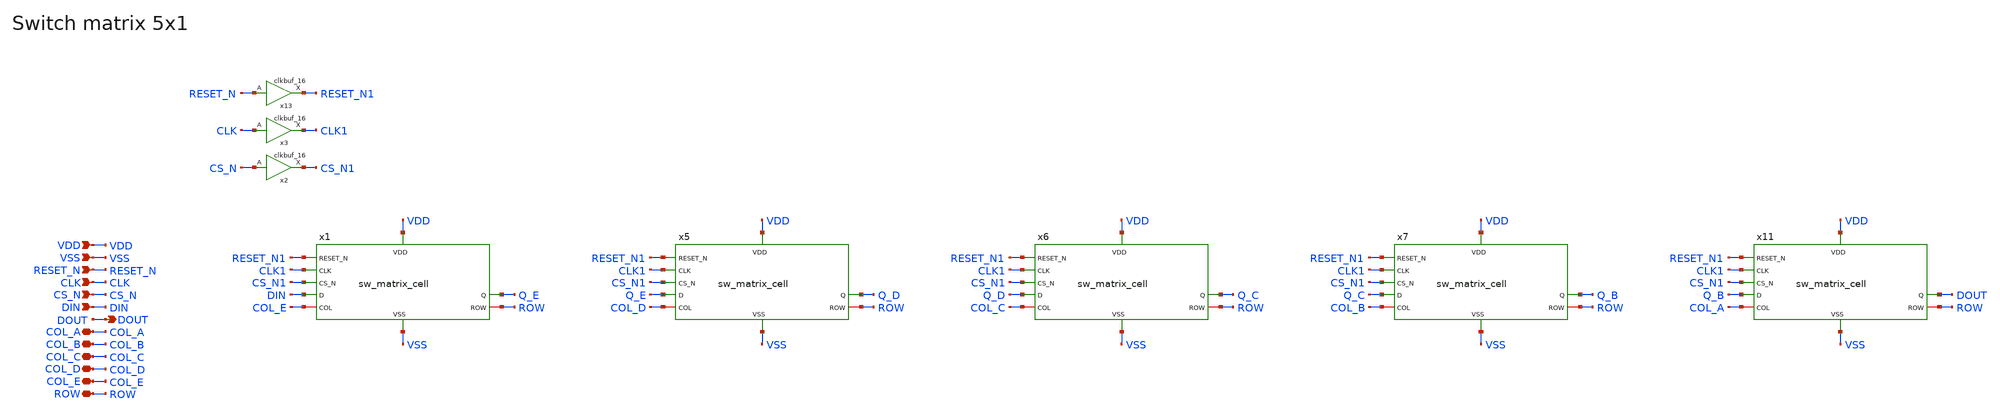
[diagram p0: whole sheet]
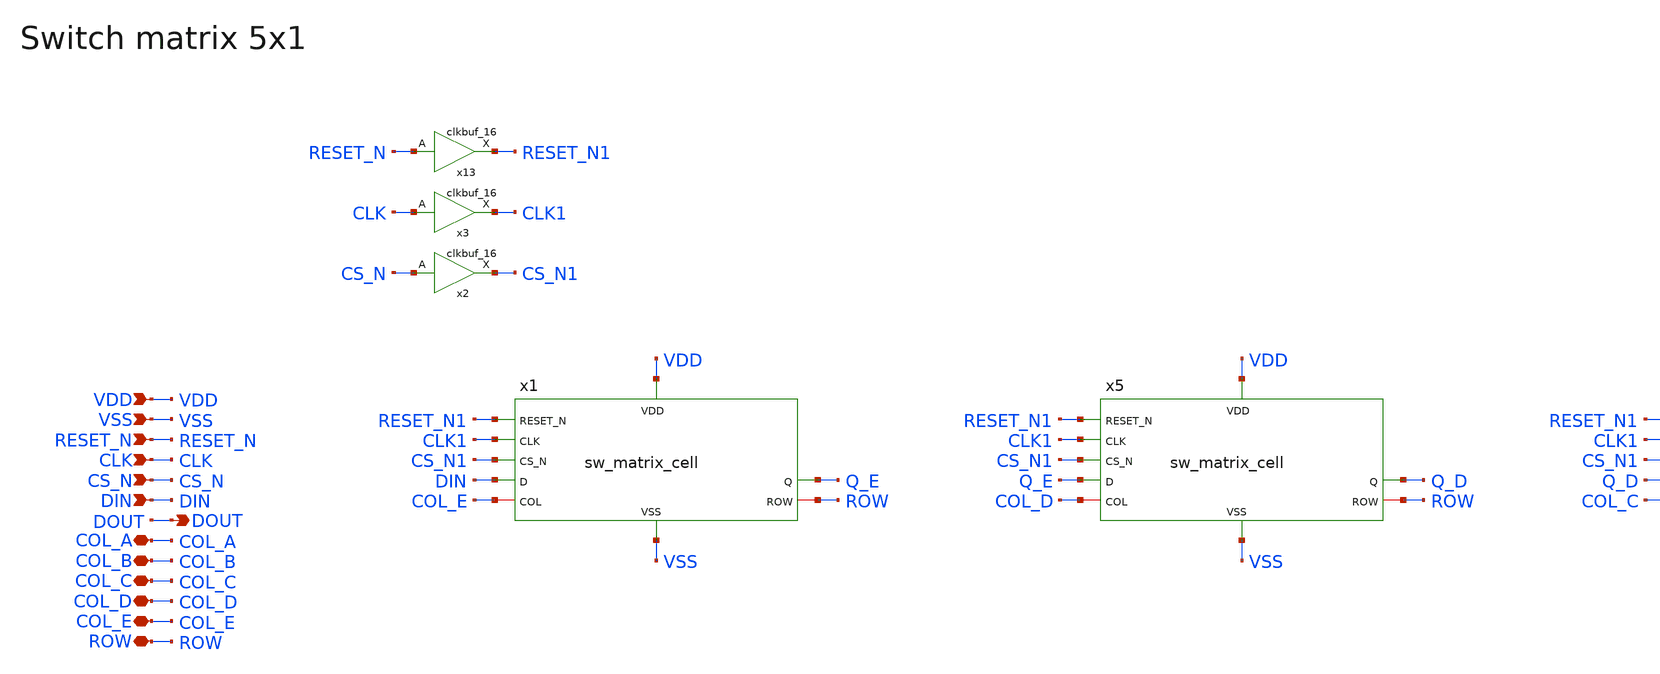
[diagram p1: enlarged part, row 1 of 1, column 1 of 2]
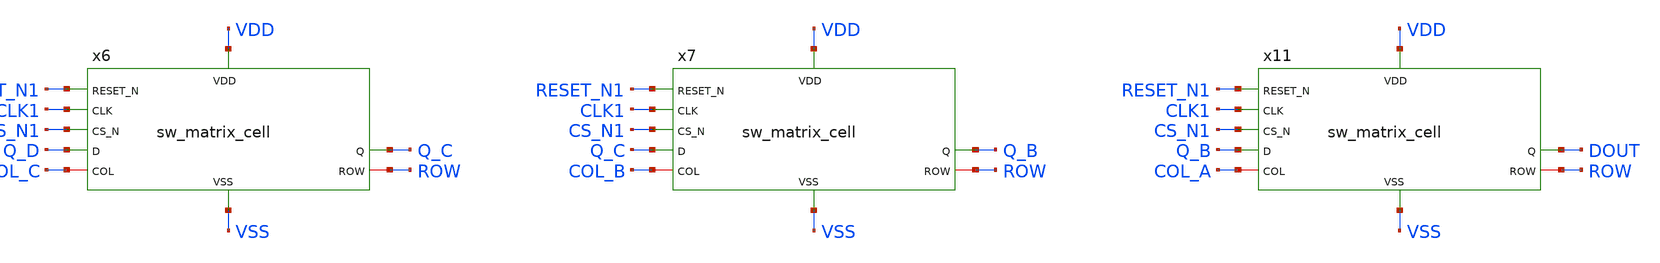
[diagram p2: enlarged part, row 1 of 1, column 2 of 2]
** sch_path: designs/libs/core_analog/sw_matrix/sw_matrix_5x1.sch
* Copyright 2022 GlobalFoundries PDK Authors
* Licensed under the Apache License, Version 2.0 (the "License");
* you may not use this file except in compliance with the License.
* You may obtain a copy of the License at
* https://www.apache.org/licenses/LICENSE-2.0
* Unless required by applicable law or agreed to in writing, software
* distributed under the License is distributed on an "AS IS" BASIS,
* WITHOUT WARRANTIES OR CONDITIONS OF ANY KIND, either express or implied.
* See the License for the specific language governing permissions and
* limitations under the License.
**.subckt sw_matrix_5x1 VDD VSS RESET_N CLK CS_N DIN COL_A COL_B COL_C COL_D ROW DOUT COL_E
*.ipin VDD
*.ipin VSS
*.ipin RESET_N
*.ipin CLK
*.ipin CS_N
*.ipin DIN
*.iopin COL_A
*.iopin COL_B
*.iopin COL_C
*.iopin COL_D
*.iopin ROW
*.opin DOUT
*.iopin COL_E
x1 VDD VSS RESET_N1 CLK1 DIN CS_N1 Q_E COL_E ROW sw_matrix_cell
x5 VDD VSS RESET_N1 CLK1 Q_E CS_N1 Q_D COL_D ROW sw_matrix_cell
x6 VDD VSS RESET_N1 CLK1 Q_D CS_N1 Q_C COL_C ROW sw_matrix_cell
x7 VDD VSS RESET_N1 CLK1 Q_C CS_N1 Q_B COL_B ROW sw_matrix_cell
x11 VDD VSS RESET_N1 CLK1 Q_B CS_N1 DOUT COL_A ROW sw_matrix_cell
x3 CLK CLK1 VDD VDD VSS VSS gf180mcu_fd_sc_mcu7t5v0__clkbuf_16
x13 RESET_N RESET_N1 VDD VDD VSS VSS gf180mcu_fd_sc_mcu7t5v0__clkbuf_16
x2 CS_N CS_N1 VDD VDD VSS VSS gf180mcu_fd_sc_mcu7t5v0__clkbuf_16
**** begin user architecture code

.include /foss/pdks/gf180mcuD/libs.ref/gf180mcu_fd_sc_mcu7t5v0/spice/gf180mcu_fd_sc_mcu7t5v0.spice


**** end user architecture code
**.ends
.end
